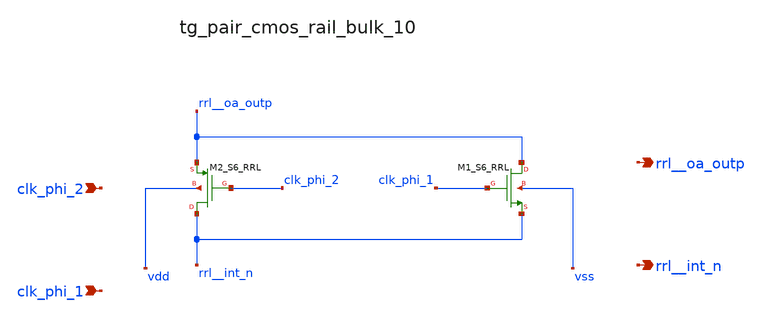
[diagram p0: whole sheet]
** sch_path: analog-db/raw/ia_004_fan_chopper_rrl/hier/blocks/tg_pair_cmos_rail_bulk_10.sch
**.subckt tg_pair_cmos_rail_bulk_10 clk_phi_2 clk_phi_1 rrl__oa_outp rrl__int_n
*.ipin clk_phi_2
*.ipin clk_phi_1
*.opin rrl__oa_outp
*.opin rrl__int_n
XM1_S6_RRL rrl__oa_outp clk_phi_1 rrl__int_n vss sg13_lv_nmos w=x_dut_xm1_s6_rrl_w
+ l=x_dut_xm1_s6_rrl_l ng=1 m=x_dut_xm1_s6_rrl_m
XM2_S6_RRL rrl__int_n clk_phi_2 rrl__oa_outp vdd sg13_lv_pmos w=x_dut_xm2_s6_rrl_w
+ l=x_dut_xm2_s6_rrl_l ng=1 m=x_dut_xm2_s6_rrl_m
**.ends
.end
